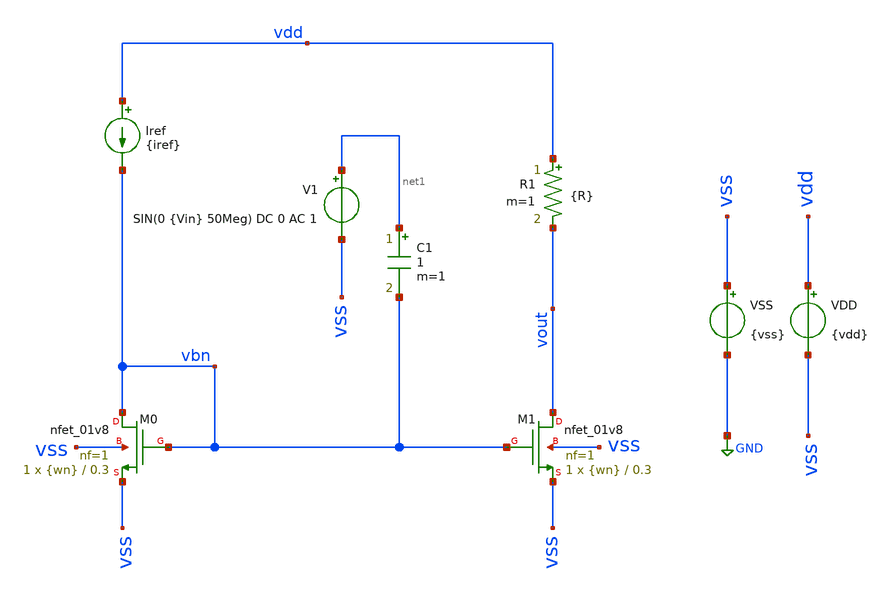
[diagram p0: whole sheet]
** sch_path: Tp2/Mis Simulaciones/tp2_5b.sch
**.subckt tp2_5b
Iref vdd vbn {iref}
VSS vss GND {vss}
VDD vdd vss {vdd}
V1 net1 vss SIN(0 {Vin} 50Meg) DC 0 AC 1
XM1 vout vbn vss vss sky130_fd_pr__nfet_01v8 L=0.3 W={wn} nf=1 ad='int((nf+1)/2) * W/nf * 0.29' as='int((nf+2)/2) * W/nf * 0.29'
+ pd='2*int((nf+1)/2) * (W/nf + 0.29)' ps='2*int((nf+2)/2) * (W/nf + 0.29)' nrd='0.29 / W' nrs='0.29 / W'
+ sa=0 sb=0 sd=0 mult=1 m=1
XM0 vbn vbn vss vss sky130_fd_pr__nfet_01v8 L=0.3 W={wn} nf=1 ad='int((nf+1)/2) * W/nf * 0.29' as='int((nf+2)/2) * W/nf * 0.29'
+ pd='2*int((nf+1)/2) * (W/nf + 0.29)' ps='2*int((nf+2)/2) * (W/nf + 0.29)' nrd='0.29 / W' nrs='0.29 / W'
+ sa=0 sb=0 sd=0 mult=1 m=1
C1 net1 vbn 1 m=1
R1 vdd vout {R} m=1
**** begin user architecture code



* Parameters
.param vdd = 1.8
.param vss = 0.0
.param iref = 200u
.param wn = 6.5
.param R = 4.5k
.param Vin = 150m

.options TEMP = 65.0

* Models
.lib ~/skywater/skywater-pdk/libraries/sky130_fd_pr_ngspice/latest/models/corners/sky130.lib TT

* Data to save
.save all  @M.XM0.msky130_fd_pr__nfet_01v8[id]  @M.XM0.msky130_fd_pr__nfet_01v8[vds]  @M.XM0.msky130_fd_pr__nfet_01v8[vgs]  @M.XM0.msky130_fd_pr__nfet_01v8[vdsat]  @M.XM0.msky130_fd_pr__nfet_01v8[vth]  @M.XM0.msky130_fd_pr__nfet_01v8[gm]  @M.XM1.msky130_fd_pr__nfet_01v8[id]  @M.XM1.msky130_fd_pr__nfet_01v8[vds]  @M.XM1.msky130_fd_pr__nfet_01v8[vgs]  @M.XM1.msky130_fd_pr__nfet_01v8[vdsat]  @M.XM1.msky130_fd_pr__nfet_01v8[vth]  @M.XM1.msky130_fd_pr__nfet_01v8[gm]  @M.XM1.msky130_fd_pr__nfet_01v8[gds]

* Simulation
.control
  ac dec 100 10k 100G
  setplot ac1
  plot vdb(vout) {vp(vout)*180/PI}
  write tp2_5b_ac.raw

  reset
  tran 0.01n 100n
  plot v(vbn) v(vout)
  write tp2_5b_tran.raw

  reset
  op
  save all
  print all
  unset filetype
  write tp2_5b.raw
.endc

.end


**** end user architecture code
**.ends
.GLOBAL GND
.end
